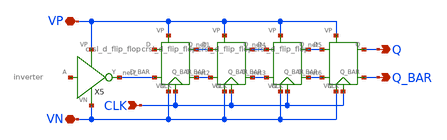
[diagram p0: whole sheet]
** sch_path: mp2/schematics/untitled.sch
**.subckt untitled VP VN CLK Q Q_BAR
*.iopin VP
*.iopin VN
*.ipin CLK
*.opin Q
*.opin Q_BAR
X4 net5 net6 Q_BAR VP Q CLK VN crsl_d_flip_flop
X1 net8 net7 net2 VP net1 CLK VN crsl_d_flip_flop
X2 net1 net2 net3 VP net4 CLK VN crsl_d_flip_flop
X3 net4 net3 net6 VP net5 CLK VN crsl_d_flip_flop
X5 net9 VP VN net7 inverter
**.ends

* expanding   symbol:  /home/madvlsi/Documents/VLSI/mp2/schematics/crsl_d_flip_flop.sym # of pins=7
** sym_path: mp2/schematics/crsl_d_flip_flop.sym
** sch_path: mp2/schematics/crsl_d_flip_flop.sch
.subckt crsl_d_flip_flop D D_BAR Q_BAR VP Q CLK VN
*.ipin D
*.ipin D_BAR
*.iopin VP
*.iopin VN
*.opin Q
*.opin Q_BAR
*.ipin CLK
XM1 net1 CLK D VP sky130_fd_pr__pfet_01v8 L=0.15 W=1 nf=1 ad='int((nf+1)/2) * W/nf * 0.29' as='int((nf+2)/2) * W/nf * 0.29'
+ pd='2*int((nf+1)/2) * (W/nf + 0.29)' ps='2*int((nf+2)/2) * (W/nf + 0.29)' nrd='0.29 / W' nrs='0.29 / W'
+ sa=0 sb=0 sd=0 mult=1 m=1
XM2 net2 CLK D_BAR VP sky130_fd_pr__pfet_01v8 L=0.15 W=1 nf=1 ad='int((nf+1)/2) * W/nf * 0.29' as='int((nf+2)/2) * W/nf * 0.29'
+ pd='2*int((nf+1)/2) * (W/nf + 0.29)' ps='2*int((nf+2)/2) * (W/nf + 0.29)' nrd='0.29 / W' nrs='0.29 / W'
+ sa=0 sb=0 sd=0 mult=1 m=1
XM8 net2 net1 VP VP sky130_fd_pr__pfet_01v8 L=0.15 W=1 nf=1 ad='int((nf+1)/2) * W/nf * 0.29' as='int((nf+2)/2) * W/nf * 0.29'
+ pd='2*int((nf+1)/2) * (W/nf + 0.29)' ps='2*int((nf+2)/2) * (W/nf + 0.29)' nrd='0.29 / W' nrs='0.29 / W'
+ sa=0 sb=0 sd=0 mult=1 m=1
XM9 VP net2 net1 VP sky130_fd_pr__pfet_01v8 L=0.15 W=1 nf=1 ad='int((nf+1)/2) * W/nf * 0.29' as='int((nf+2)/2) * W/nf * 0.29'
+ pd='2*int((nf+1)/2) * (W/nf + 0.29)' ps='2*int((nf+2)/2) * (W/nf + 0.29)' nrd='0.29 / W' nrs='0.29 / W'
+ sa=0 sb=0 sd=0 mult=1 m=1
XM6 net2 net1 net3 VN sky130_fd_pr__nfet_01v8 L=0.15 W=1 nf=1 ad='int((nf+1)/2) * W/nf * 0.29' as='int((nf+2)/2) * W/nf * 0.29'
+ pd='2*int((nf+1)/2) * (W/nf + 0.29)' ps='2*int((nf+2)/2) * (W/nf + 0.29)' nrd='0.29 / W' nrs='0.29 / W'
+ sa=0 sb=0 sd=0 mult=1 m=1
XM7 net3 net2 net1 VN sky130_fd_pr__nfet_01v8 L=0.15 W=1 nf=1 ad='int((nf+1)/2) * W/nf * 0.29' as='int((nf+2)/2) * W/nf * 0.29'
+ pd='2*int((nf+1)/2) * (W/nf + 0.29)' ps='2*int((nf+2)/2) * (W/nf + 0.29)' nrd='0.29 / W' nrs='0.29 / W'
+ sa=0 sb=0 sd=0 mult=1 m=1
XM3 Q CLK net1 VN sky130_fd_pr__nfet_01v8 L=0.15 W=1 nf=1 ad='int((nf+1)/2) * W/nf * 0.29' as='int((nf+2)/2) * W/nf * 0.29'
+ pd='2*int((nf+1)/2) * (W/nf + 0.29)' ps='2*int((nf+2)/2) * (W/nf + 0.29)' nrd='0.29 / W' nrs='0.29 / W'
+ sa=0 sb=0 sd=0 mult=1 m=1
XM4 Q_BAR CLK net2 VN sky130_fd_pr__nfet_01v8 L=0.15 W=1 nf=1 ad='int((nf+1)/2) * W/nf * 0.29' as='int((nf+2)/2) * W/nf * 0.29'
+ pd='2*int((nf+1)/2) * (W/nf + 0.29)' ps='2*int((nf+2)/2) * (W/nf + 0.29)' nrd='0.29 / W' nrs='0.29 / W'
+ sa=0 sb=0 sd=0 mult=1 m=1
XM13 Q_BAR Q VN VN sky130_fd_pr__nfet_01v8 L=0.15 W=1 nf=1 ad='int((nf+1)/2) * W/nf * 0.29' as='int((nf+2)/2) * W/nf * 0.29'
+ pd='2*int((nf+1)/2) * (W/nf + 0.29)' ps='2*int((nf+2)/2) * (W/nf + 0.29)' nrd='0.29 / W' nrs='0.29 / W'
+ sa=0 sb=0 sd=0 mult=1 m=1
XM14 VN Q_BAR Q VN sky130_fd_pr__nfet_01v8 L=0.15 W=1 nf=1 ad='int((nf+1)/2) * W/nf * 0.29' as='int((nf+2)/2) * W/nf * 0.29'
+ pd='2*int((nf+1)/2) * (W/nf + 0.29)' ps='2*int((nf+2)/2) * (W/nf + 0.29)' nrd='0.29 / W' nrs='0.29 / W'
+ sa=0 sb=0 sd=0 mult=1 m=1
XM12 net4 Q_BAR Q VP sky130_fd_pr__pfet_01v8 L=0.15 W=1 nf=1 ad='int((nf+1)/2) * W/nf * 0.29' as='int((nf+2)/2) * W/nf * 0.29'
+ pd='2*int((nf+1)/2) * (W/nf + 0.29)' ps='2*int((nf+2)/2) * (W/nf + 0.29)' nrd='0.29 / W' nrs='0.29 / W'
+ sa=0 sb=0 sd=0 mult=1 m=1
XM11 Q_BAR Q net4 VP sky130_fd_pr__pfet_01v8 L=0.15 W=1 nf=1 ad='int((nf+1)/2) * W/nf * 0.29' as='int((nf+2)/2) * W/nf * 0.29'
+ pd='2*int((nf+1)/2) * (W/nf + 0.29)' ps='2*int((nf+2)/2) * (W/nf + 0.29)' nrd='0.29 / W' nrs='0.29 / W'
+ sa=0 sb=0 sd=0 mult=1 m=1
XM5 net3 CLK VN VN sky130_fd_pr__nfet_01v8 L=0.15 W=4 nf=1 ad='int((nf+1)/2) * W/nf * 0.29' as='int((nf+2)/2) * W/nf * 0.29'
+ pd='2*int((nf+1)/2) * (W/nf + 0.29)' ps='2*int((nf+2)/2) * (W/nf + 0.29)' nrd='0.29 / W' nrs='0.29 / W'
+ sa=0 sb=0 sd=0 mult=1 m=1
XM10 net4 CLK VP VP sky130_fd_pr__pfet_01v8 L=0.15 W=1 nf=1 ad='int((nf+1)/2) * W/nf * 0.29' as='int((nf+2)/2) * W/nf * 0.29'
+ pd='2*int((nf+1)/2) * (W/nf + 0.29)' ps='2*int((nf+2)/2) * (W/nf + 0.29)' nrd='0.29 / W' nrs='0.29 / W'
+ sa=0 sb=0 sd=0 mult=1 m=1
.ends


* expanding   symbol:  /home/madvlsi/Documents/VLSI/mp2/schematics/inverter.sym # of pins=4
** sym_path: mp2/schematics/inverter.sym
** sch_path: mp2/schematics/inverter.sch
.subckt inverter A VP VN Y
*.ipin A
*.iopin VP
*.iopin VN
*.opin Y
XM2 Y A VP VP sky130_fd_pr__pfet_01v8 L=0.15 W=1 nf=1 ad='int((nf+1)/2) * W/nf * 0.29' as='int((nf+2)/2) * W/nf * 0.29'
+ pd='2*int((nf+1)/2) * (W/nf + 0.29)' ps='2*int((nf+2)/2) * (W/nf + 0.29)' nrd='0.29 / W' nrs='0.29 / W'
+ sa=0 sb=0 sd=0 mult=1 m=1
XM1 Y A VN VN sky130_fd_pr__nfet_01v8 L=0.15 W=1 nf=1 ad='int((nf+1)/2) * W/nf * 0.29' as='int((nf+2)/2) * W/nf * 0.29'
+ pd='2*int((nf+1)/2) * (W/nf + 0.29)' ps='2*int((nf+2)/2) * (W/nf + 0.29)' nrd='0.29 / W' nrs='0.29 / W'
+ sa=0 sb=0 sd=0 mult=1 m=1
.ends

.end
